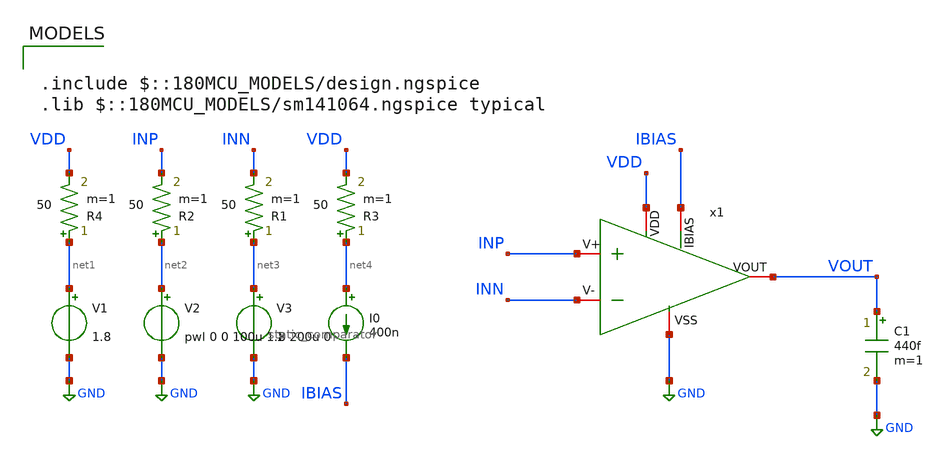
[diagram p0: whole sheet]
** sch_path: designs/static_comparator/xschem/static_comparator_tb_tran.sch
**.subckt static_comparator_tb_tran
V1 net1 GND 1.8
V2 net2 GND pwl 0 0 100u 1.8 200u 0
C1 VOUT GND 440f m=1
V3 net3 GND 1
I0 net4 IBIAS 400n
x1 VDD IBIAS GND INP INN VOUT static_comparator
R3 net4 VDD 50 m=1
R1 net3 INN 50 m=1
R2 net2 INP 50 m=1
R4 net1 VDD 50 m=1
**** begin user architecture code

.include $::180MCU_MODELS/design.ngspice
.lib $::180MCU_MODELS/sm141064.ngspice typical




.control
save all

** Simulación transitoria
tran 1u 200u

setplot tran1
let vin  = v(INP)
let vref = v(INN)
let vout = v(VOUT)
plot vout vin vref

write comparator_tb_tran.raw
.endc


**** end user architecture code
**.ends

* expanding   symbol:  gf180/static_comparator/xschem/static_comparator.sym # of pins=6
** sym_path: gf180/static_comparator/xschem/static_comparator.sym
** sch_path: gf180/static_comparator/xschem/static_comparator.sch
.subckt static_comparator VDD IBIAS VSS V+ V- VOUT
*.iopin IBIAS
*.iopin VSS
*.iopin VDD
*.iopin V+
*.iopin V-
*.iopin VOUT
XM1 IBIAS IBIAS VSS VSS nfet_03v3 L=4u W=1.1u nf=1 ad='int((nf+1)/2) * W/nf * 0.18u' as='int((nf+2)/2) * W/nf * 0.18u'
+ pd='2*int((nf+1)/2) * (W/nf + 0.18u)' ps='2*int((nf+2)/2) * (W/nf + 0.18u)' nrd='0.18u / W' nrs='0.18u / W'
+ sa=0 sb=0 sd=0 m=1
XM3 net1 net1 VDD VDD pfet_03v3 L=2u W=4.5u nf=1 ad='int((nf+1)/2) * W/nf * 0.18u' as='int((nf+2)/2) * W/nf * 0.18u'
+ pd='2*int((nf+1)/2) * (W/nf + 0.18u)' ps='2*int((nf+2)/2) * (W/nf + 0.18u)' nrd='0.18u / W' nrs='0.18u / W'
+ sa=0 sb=0 sd=0 m=1
XM2 net1 IBIAS VSS VSS nfet_03v3 L=4u W=625n nf=1 ad='int((nf+1)/2) * W/nf * 0.18u' as='int((nf+2)/2) * W/nf * 0.18u'
+ pd='2*int((nf+1)/2) * (W/nf + 0.18u)' ps='2*int((nf+2)/2) * (W/nf + 0.18u)' nrd='0.18u / W' nrs='0.18u / W'
+ sa=0 sb=0 sd=0 m=1
XM4 net2 net1 VDD VDD pfet_03v3 L=2u W=25u nf=1 ad='int((nf+1)/2) * W/nf * 0.18u' as='int((nf+2)/2) * W/nf * 0.18u'
+ pd='2*int((nf+1)/2) * (W/nf + 0.18u)' ps='2*int((nf+2)/2) * (W/nf + 0.18u)' nrd='0.18u / W' nrs='0.18u / W'
+ sa=0 sb=0 sd=0 m=1
XM5 Vx+ V+ net2 VDD pfet_03v3 L=360n W=2u nf=1 ad='int((nf+1)/2) * W/nf * 0.18u' as='int((nf+2)/2) * W/nf * 0.18u'
+ pd='2*int((nf+1)/2) * (W/nf + 0.18u)' ps='2*int((nf+2)/2) * (W/nf + 0.18u)' nrd='0.18u / W' nrs='0.18u / W'
+ sa=0 sb=0 sd=0 m=10
XM7 Vx+ Vx+ VSS VSS nfet_03v3 L=2u W=985n nf=1 ad='int((nf+1)/2) * W/nf * 0.18u' as='int((nf+2)/2) * W/nf * 0.18u'
+ pd='2*int((nf+1)/2) * (W/nf + 0.18u)' ps='2*int((nf+2)/2) * (W/nf + 0.18u)' nrd='0.18u / W' nrs='0.18u / W'
+ sa=0 sb=0 sd=0 m=1
XM6 Vx- V- net2 VDD pfet_03v3 L=360n W=2u nf=1 ad='int((nf+1)/2) * W/nf * 0.18u' as='int((nf+2)/2) * W/nf * 0.18u'
+ pd='2*int((nf+1)/2) * (W/nf + 0.18u)' ps='2*int((nf+2)/2) * (W/nf + 0.18u)' nrd='0.18u / W' nrs='0.18u / W'
+ sa=0 sb=0 sd=0 m=10
XM8 Vx- Vx- VSS VSS nfet_03v3 L=2u W=985n nf=1 ad='int((nf+1)/2) * W/nf * 0.18u' as='int((nf+2)/2) * W/nf * 0.18u'
+ pd='2*int((nf+1)/2) * (W/nf + 0.18u)' ps='2*int((nf+2)/2) * (W/nf + 0.18u)' nrd='0.18u / W' nrs='0.18u / W'
+ sa=0 sb=0 sd=0 m=1
XM9 net3 net3 VDD VDD pfet_03v3 L=4u W=950n nf=1 ad='int((nf+1)/2) * W/nf * 0.18u' as='int((nf+2)/2) * W/nf * 0.18u'
+ pd='2*int((nf+1)/2) * (W/nf + 0.18u)' ps='2*int((nf+2)/2) * (W/nf + 0.18u)' nrd='0.18u / W' nrs='0.18u / W'
+ sa=0 sb=0 sd=0 m=1
XM10 VOUT net3 VDD VDD pfet_03v3 L=4u W=950n nf=1 ad='int((nf+1)/2) * W/nf * 0.18u' as='int((nf+2)/2) * W/nf * 0.18u'
+ pd='2*int((nf+1)/2) * (W/nf + 0.18u)' ps='2*int((nf+2)/2) * (W/nf + 0.18u)' nrd='0.18u / W' nrs='0.18u / W'
+ sa=0 sb=0 sd=0 m=1
XM11 net3 Vx- VSS VSS nfet_03v3 L=2u W=1.1u nf=1 ad='int((nf+1)/2) * W/nf * 0.18u' as='int((nf+2)/2) * W/nf * 0.18u'
+ pd='2*int((nf+1)/2) * (W/nf + 0.18u)' ps='2*int((nf+2)/2) * (W/nf + 0.18u)' nrd='0.18u / W' nrs='0.18u / W'
+ sa=0 sb=0 sd=0 m=1
XM12 VOUT Vx+ VSS VSS nfet_03v3 L=2u W=1.1u nf=1 ad='int((nf+1)/2) * W/nf * 0.18u' as='int((nf+2)/2) * W/nf * 0.18u'
+ pd='2*int((nf+1)/2) * (W/nf + 0.18u)' ps='2*int((nf+2)/2) * (W/nf + 0.18u)' nrd='0.18u / W' nrs='0.18u / W'
+ sa=0 sb=0 sd=0 m=1
.ends

.GLOBAL GND
.end
